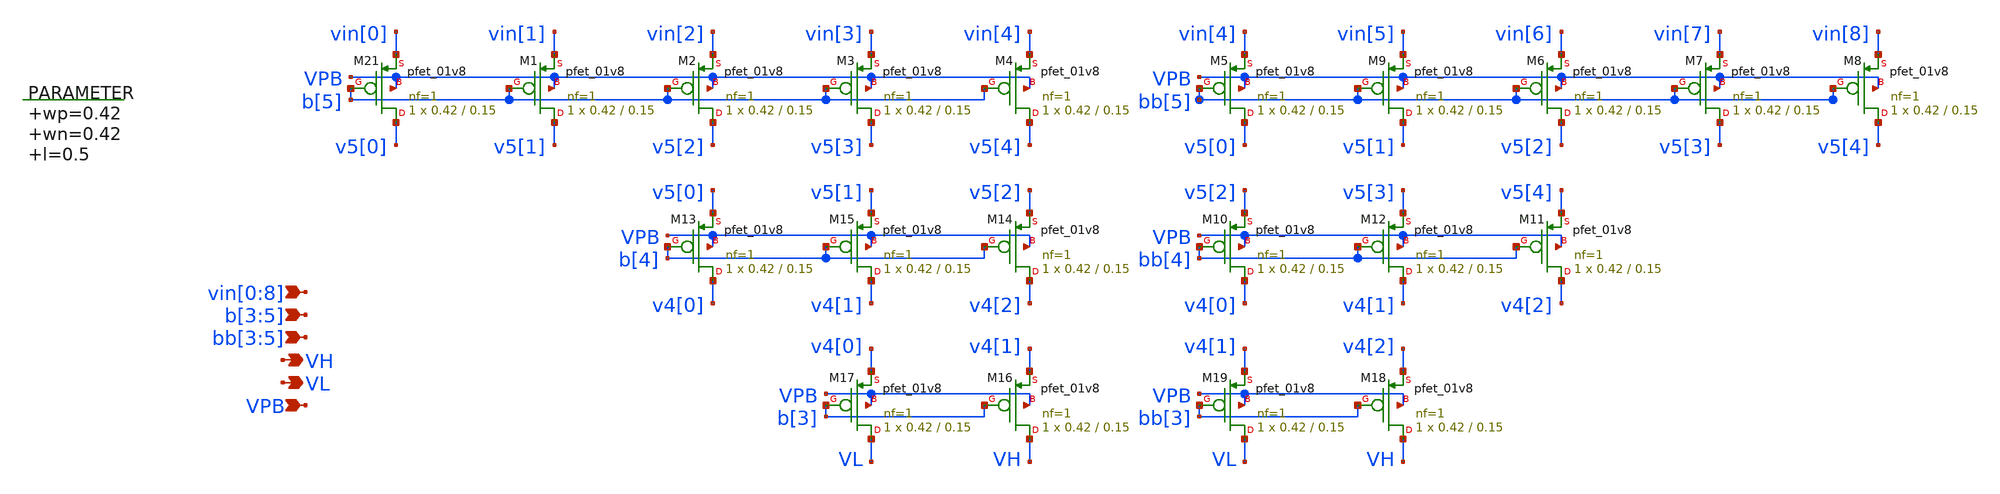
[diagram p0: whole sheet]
** sch_path: xschem/vselector_3b_2v.sch
**.subckt vselector_3b_2v vin[0],vin[1],vin[2],vin[3],vin[4],vin[5],vin[6],vin[7],vin[8] VH VPB
*+ b[3],b[4],b[5] VL bb[3],bb[4],bb[5]
*.ipin vin[0],vin[1],vin[2],vin[3],vin[4],vin[5],vin[6],vin[7],vin[8]
*.opin VH
*.ipin VPB
*.ipin b[3],b[4],b[5]
*.opin VL
*.ipin bb[3],bb[4],bb[5]
.param wp=0.42 wn=0.42 l=0.5

XM21 v5[0] b[5] vin[0] VPB sky130_fd_pr__pfet_01v8 L=0.15 W=0.42 nf=1 ad='int((nf+1)/2) * W/nf * 0.29'
+ as='int((nf+2)/2) * W/nf * 0.29' pd='2*int((nf+1)/2) * (W/nf + 0.29)' ps='2*int((nf+2)/2) * (W/nf + 0.29)'
+ nrd='0.29 / W' nrs='0.29 / W' sa=0 sb=0 sd=0 mult=1 m=1
XM1 v5[1] b[5] vin[1] VPB sky130_fd_pr__pfet_01v8 L=0.15 W=0.42 nf=1 ad='int((nf+1)/2) * W/nf * 0.29'
+ as='int((nf+2)/2) * W/nf * 0.29' pd='2*int((nf+1)/2) * (W/nf + 0.29)' ps='2*int((nf+2)/2) * (W/nf + 0.29)'
+ nrd='0.29 / W' nrs='0.29 / W' sa=0 sb=0 sd=0 mult=1 m=1
XM2 v5[2] b[5] vin[2] VPB sky130_fd_pr__pfet_01v8 L=0.15 W=0.42 nf=1 ad='int((nf+1)/2) * W/nf * 0.29'
+ as='int((nf+2)/2) * W/nf * 0.29' pd='2*int((nf+1)/2) * (W/nf + 0.29)' ps='2*int((nf+2)/2) * (W/nf + 0.29)'
+ nrd='0.29 / W' nrs='0.29 / W' sa=0 sb=0 sd=0 mult=1 m=1
XM3 v5[3] b[5] vin[3] VPB sky130_fd_pr__pfet_01v8 L=0.15 W=0.42 nf=1 ad='int((nf+1)/2) * W/nf * 0.29'
+ as='int((nf+2)/2) * W/nf * 0.29' pd='2*int((nf+1)/2) * (W/nf + 0.29)' ps='2*int((nf+2)/2) * (W/nf + 0.29)'
+ nrd='0.29 / W' nrs='0.29 / W' sa=0 sb=0 sd=0 mult=1 m=1
XM4 v5[4] b[5] vin[4] VPB sky130_fd_pr__pfet_01v8 L=0.15 W=0.42 nf=1 ad='int((nf+1)/2) * W/nf * 0.29'
+ as='int((nf+2)/2) * W/nf * 0.29' pd='2*int((nf+1)/2) * (W/nf + 0.29)' ps='2*int((nf+2)/2) * (W/nf + 0.29)'
+ nrd='0.29 / W' nrs='0.29 / W' sa=0 sb=0 sd=0 mult=1 m=1
XM5 v5[0] bb[5] vin[4] VPB sky130_fd_pr__pfet_01v8 L=0.15 W=0.42 nf=1 ad='int((nf+1)/2) * W/nf * 0.29'
+ as='int((nf+2)/2) * W/nf * 0.29' pd='2*int((nf+1)/2) * (W/nf + 0.29)' ps='2*int((nf+2)/2) * (W/nf + 0.29)'
+ nrd='0.29 / W' nrs='0.29 / W' sa=0 sb=0 sd=0 mult=1 m=1
XM6 v5[2] bb[5] vin[6] VPB sky130_fd_pr__pfet_01v8 L=0.15 W=0.42 nf=1 ad='int((nf+1)/2) * W/nf * 0.29'
+ as='int((nf+2)/2) * W/nf * 0.29' pd='2*int((nf+1)/2) * (W/nf + 0.29)' ps='2*int((nf+2)/2) * (W/nf + 0.29)'
+ nrd='0.29 / W' nrs='0.29 / W' sa=0 sb=0 sd=0 mult=1 m=1
XM7 v5[3] bb[5] vin[7] VPB sky130_fd_pr__pfet_01v8 L=0.15 W=0.42 nf=1 ad='int((nf+1)/2) * W/nf * 0.29'
+ as='int((nf+2)/2) * W/nf * 0.29' pd='2*int((nf+1)/2) * (W/nf + 0.29)' ps='2*int((nf+2)/2) * (W/nf + 0.29)'
+ nrd='0.29 / W' nrs='0.29 / W' sa=0 sb=0 sd=0 mult=1 m=1
XM8 v5[4] bb[5] vin[8] VPB sky130_fd_pr__pfet_01v8 L=0.15 W=0.42 nf=1 ad='int((nf+1)/2) * W/nf * 0.29'
+ as='int((nf+2)/2) * W/nf * 0.29' pd='2*int((nf+1)/2) * (W/nf + 0.29)' ps='2*int((nf+2)/2) * (W/nf + 0.29)'
+ nrd='0.29 / W' nrs='0.29 / W' sa=0 sb=0 sd=0 mult=1 m=1
XM9 v5[1] bb[5] vin[5] VPB sky130_fd_pr__pfet_01v8 L=0.15 W=0.42 nf=1 ad='int((nf+1)/2) * W/nf * 0.29'
+ as='int((nf+2)/2) * W/nf * 0.29' pd='2*int((nf+1)/2) * (W/nf + 0.29)' ps='2*int((nf+2)/2) * (W/nf + 0.29)'
+ nrd='0.29 / W' nrs='0.29 / W' sa=0 sb=0 sd=0 mult=1 m=1
XM10 v4[0] bb[4] v5[2] VPB sky130_fd_pr__pfet_01v8 L=0.15 W=0.42 nf=1 ad='int((nf+1)/2) * W/nf * 0.29'
+ as='int((nf+2)/2) * W/nf * 0.29' pd='2*int((nf+1)/2) * (W/nf + 0.29)' ps='2*int((nf+2)/2) * (W/nf + 0.29)'
+ nrd='0.29 / W' nrs='0.29 / W' sa=0 sb=0 sd=0 mult=1 m=1
XM11 v4[2] bb[4] v5[4] VPB sky130_fd_pr__pfet_01v8 L=0.15 W=0.42 nf=1 ad='int((nf+1)/2) * W/nf * 0.29'
+ as='int((nf+2)/2) * W/nf * 0.29' pd='2*int((nf+1)/2) * (W/nf + 0.29)' ps='2*int((nf+2)/2) * (W/nf + 0.29)'
+ nrd='0.29 / W' nrs='0.29 / W' sa=0 sb=0 sd=0 mult=1 m=1
XM12 v4[1] bb[4] v5[3] VPB sky130_fd_pr__pfet_01v8 L=0.15 W=0.42 nf=1 ad='int((nf+1)/2) * W/nf * 0.29'
+ as='int((nf+2)/2) * W/nf * 0.29' pd='2*int((nf+1)/2) * (W/nf + 0.29)' ps='2*int((nf+2)/2) * (W/nf + 0.29)'
+ nrd='0.29 / W' nrs='0.29 / W' sa=0 sb=0 sd=0 mult=1 m=1
XM13 v4[0] b[4] v5[0] VPB sky130_fd_pr__pfet_01v8 L=0.15 W=0.42 nf=1 ad='int((nf+1)/2) * W/nf * 0.29'
+ as='int((nf+2)/2) * W/nf * 0.29' pd='2*int((nf+1)/2) * (W/nf + 0.29)' ps='2*int((nf+2)/2) * (W/nf + 0.29)'
+ nrd='0.29 / W' nrs='0.29 / W' sa=0 sb=0 sd=0 mult=1 m=1
XM14 v4[2] b[4] v5[2] VPB sky130_fd_pr__pfet_01v8 L=0.15 W=0.42 nf=1 ad='int((nf+1)/2) * W/nf * 0.29'
+ as='int((nf+2)/2) * W/nf * 0.29' pd='2*int((nf+1)/2) * (W/nf + 0.29)' ps='2*int((nf+2)/2) * (W/nf + 0.29)'
+ nrd='0.29 / W' nrs='0.29 / W' sa=0 sb=0 sd=0 mult=1 m=1
XM15 v4[1] b[4] v5[1] VPB sky130_fd_pr__pfet_01v8 L=0.15 W=0.42 nf=1 ad='int((nf+1)/2) * W/nf * 0.29'
+ as='int((nf+2)/2) * W/nf * 0.29' pd='2*int((nf+1)/2) * (W/nf + 0.29)' ps='2*int((nf+2)/2) * (W/nf + 0.29)'
+ nrd='0.29 / W' nrs='0.29 / W' sa=0 sb=0 sd=0 mult=1 m=1
XM16 VH b[3] v4[1] VPB sky130_fd_pr__pfet_01v8 L=0.15 W=0.42 nf=1 ad='int((nf+1)/2) * W/nf * 0.29' as='int((nf+2)/2) * W/nf * 0.29'
+ pd='2*int((nf+1)/2) * (W/nf + 0.29)' ps='2*int((nf+2)/2) * (W/nf + 0.29)' nrd='0.29 / W' nrs='0.29 / W'
+ sa=0 sb=0 sd=0 mult=1 m=1
XM17 VL b[3] v4[0] VPB sky130_fd_pr__pfet_01v8 L=0.15 W=0.42 nf=1 ad='int((nf+1)/2) * W/nf * 0.29' as='int((nf+2)/2) * W/nf * 0.29'
+ pd='2*int((nf+1)/2) * (W/nf + 0.29)' ps='2*int((nf+2)/2) * (W/nf + 0.29)' nrd='0.29 / W' nrs='0.29 / W'
+ sa=0 sb=0 sd=0 mult=1 m=1
XM18 VH bb[3] v4[2] VPB sky130_fd_pr__pfet_01v8 L=0.15 W=0.42 nf=1 ad='int((nf+1)/2) * W/nf * 0.29' as='int((nf+2)/2) * W/nf * 0.29'
+ pd='2*int((nf+1)/2) * (W/nf + 0.29)' ps='2*int((nf+2)/2) * (W/nf + 0.29)' nrd='0.29 / W' nrs='0.29 / W'
+ sa=0 sb=0 sd=0 mult=1 m=1
XM19 VL bb[3] v4[1] VPB sky130_fd_pr__pfet_01v8 L=0.15 W=0.42 nf=1 ad='int((nf+1)/2) * W/nf * 0.29' as='int((nf+2)/2) * W/nf * 0.29'
+ pd='2*int((nf+1)/2) * (W/nf + 0.29)' ps='2*int((nf+2)/2) * (W/nf + 0.29)' nrd='0.29 / W' nrs='0.29 / W'
+ sa=0 sb=0 sd=0 mult=1 m=1
**.ends
.end
